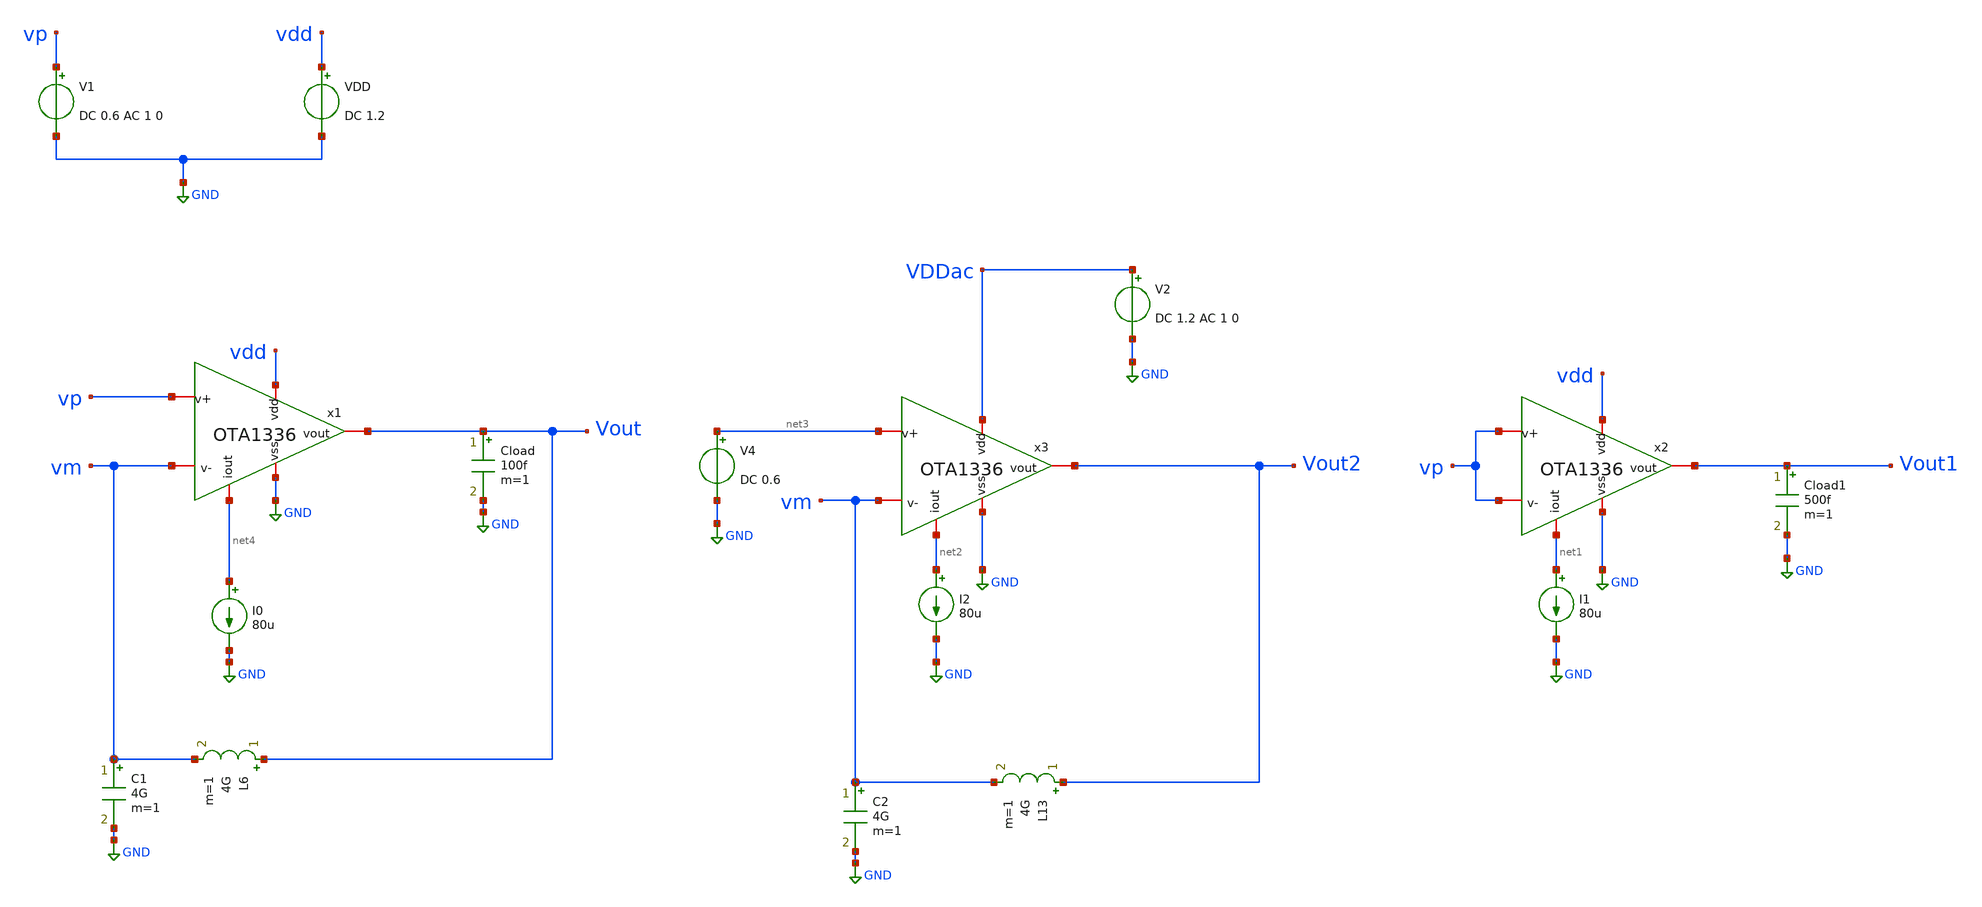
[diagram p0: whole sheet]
** sch_path: tests/data/OTA1336/testbenches/ac/xschem/OTA1336_pex_tb.sch
**.subckt OTA1336_pex_tb
V1 vp GND DC 0.6 AC 1 0
VDD vdd GND DC 1.2
I0 net4 GND 80u
Cload Vout GND 100f m=1
L6 Vout vm 4G m=1
C1 vm GND 4G m=1
I1 net1 GND 80u
Cload1 Vout1 GND 500f m=1
I2 net2 GND 80u
L13 Vout2 vm 4G m=1
C2 vm GND 4G m=1
V2 VDDac GND DC 1.2 AC 1 0
V4 net3 GND DC 0.6
x1 vdd net4 Vout vm vp GND OTA1336
x3 VDDac net2 Vout2 vm net3 GND OTA1336
x2 vdd net1 Vout1 vp vp GND OTA1336
**** begin user architecture code

.lib cornerCAP.lib cap_typ
.lib cornerMOSlv.lib mos_tt
.lib cornerRES.lib res_typ
.include ../../../../netlist/pex/OTA1336.pex.spice



*.option rseries = 1.0e-2
*.option cshunt = 1.0e-13
.control
save all
op
print v(vout) v(vp) v(vm) v(vout1) v(vout2)
write tb_OTA_op.raw
.endc

.control
op
ac dec 100 1 10e6
save all
let Av = db(v(vout) / v(vp))
let PSRR_linear = v(vout2)/v(VDDac)
let CMRR = db((v(vout)/v(vp))/(v(vout1)/v(vp)))
let phase = 180*cph(vout)/pi
write output_file.raw
.endc


**** end user architecture code
**.ends
.GLOBAL GND
.end
